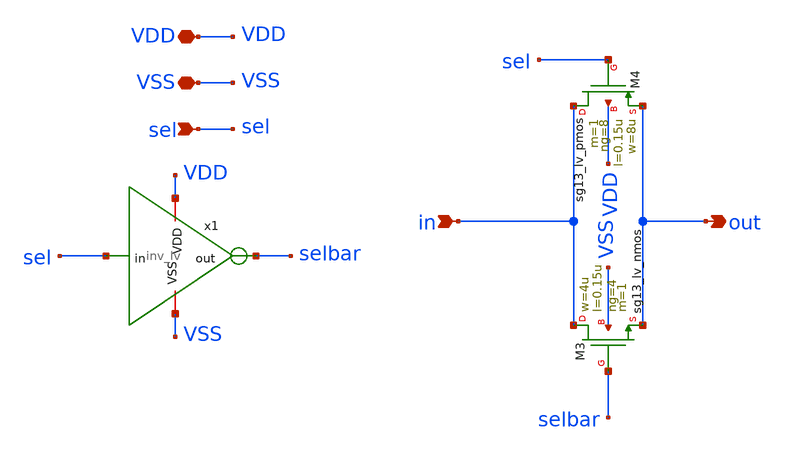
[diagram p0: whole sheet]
** sch_path: xschem/mux2I1.sch
**.subckt mux2I1 in VDD VSS out sel
*.ipin in
*.iopin VDD
*.iopin VSS
*.opin out
*.ipin sel
x1 VDD sel selbar VSS inv_lv
XM3 in selbar out VSS sg13_lv_nmos w=4u l=0.15u ng=4 m=1 mm_ok=1
XM4 in sel out VDD sg13_lv_pmos w=8u l=0.15u ng=8 m=1 mm_ok=1
**.ends

* expanding   symbol:  inv_lv.sym # of pins=4
** sym_path: inv_lv.sym
** sch_path: inv_lv.sch
.subckt inv_lv VDD in out VSS
*.ipin in
*.opin out
*.iopin VDD
*.iopin VSS
XM3 out in VDD VDD sg13_lv_pmos w=1u l=0.15u ng=1 m=1 mm_ok=1
XM4 out in VSS VSS sg13_lv_nmos w=1u l=0.15u ng=1 m=1 mm_ok=1
XMdumm1 VDD VDD VDD VDD sg13_lv_pmos w=1u l=0.15u ng=1 m=2 mm_ok=1
XMdumm2 VSS VSS VSS VSS sg13_lv_nmos w=1u l=0.15u ng=1 m=2 mm_ok=1
.ends

.end
